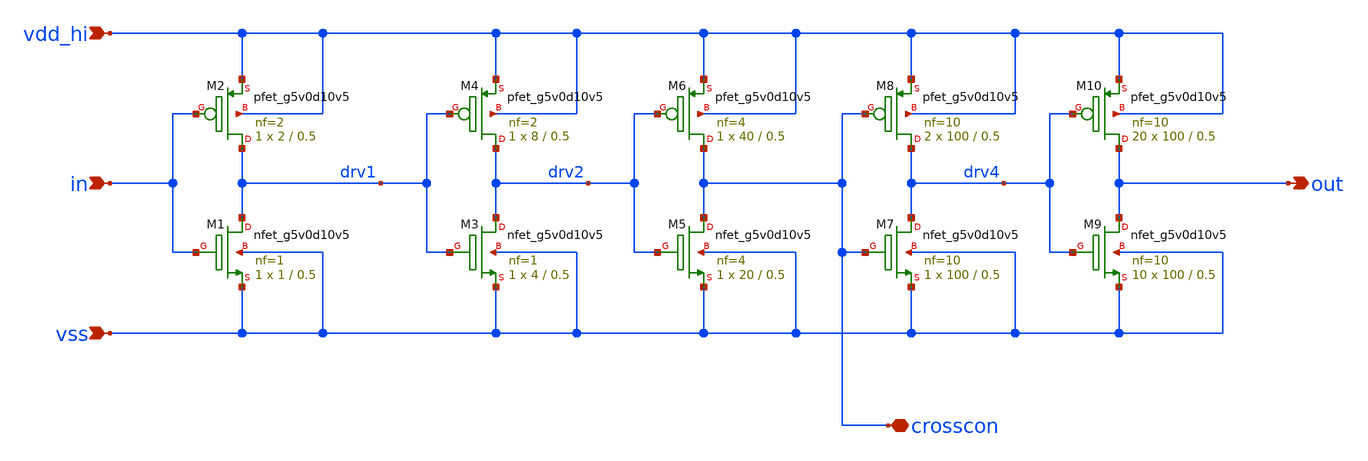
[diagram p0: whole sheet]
** sch_path: xschem/audiodac_drv_half.sch
* (c) 2022 Harald Pretl, IIC, Johannes Kepler University
**.subckt audiodac_drv_half in out vdd_hi vss crosscon
*.ipin in
*.opin out
*.ipin vdd_hi
*.ipin vss
*.iopin crosscon
XM10 out drv4 vdd_hi vdd_hi sky130_fd_pr__pfet_g5v0d10v5 L=0.5 W=100 nf=10 ad='int((10 + 1)/2) * 100 / 10 * 0.29'
+ as='int((10 + 2)/2) * 100 / 10 * 0.29' pd='2*int((10 + 1)/2) * (100 / 10 + 0.29)' ps='2*int((10 + 2)/2) * (100 / 10 + 0.29)'
+ nrd='0.29 / 100 ' nrs='0.29 / 100 ' sa=0 sb=0 sd=0 mult=20 m=20
XM9 out drv4 vss vss sky130_fd_pr__nfet_g5v0d10v5 L=0.5 W=100 nf=10 ad='int((10 + 1)/2) * 100 / 10 * 0.29'
+ as='int((10 + 2)/2) * 100 / 10 * 0.29' pd='2*int((10 + 1)/2) * (100 / 10 + 0.29)' ps='2*int((10 + 2)/2) * (100 / 10 + 0.29)'
+ nrd='0.29 / 100 ' nrs='0.29 / 100 ' sa=0 sb=0 sd=0 mult=10 m=10
XM8 drv4 crosscon vdd_hi vdd_hi sky130_fd_pr__pfet_g5v0d10v5 L=0.5 W=100 nf=10 ad='int((10 + 1)/2) * 100 / 10 * 0.29'
+ as='int((10 + 2)/2) * 100 / 10 * 0.29' pd='2*int((10 + 1)/2) * (100 / 10 + 0.29)' ps='2*int((10 + 2)/2) * (100 / 10 + 0.29)'
+ nrd='0.29 / 100 ' nrs='0.29 / 100 ' sa=0 sb=0 sd=0 mult=2 m=2
XM7 drv4 crosscon vss vss sky130_fd_pr__nfet_g5v0d10v5 L=0.5 W=100 nf=10 ad='int((10 + 1)/2) * 100 / 10 * 0.29'
+ as='int((10 + 2)/2) * 100 / 10 * 0.29' pd='2*int((10 + 1)/2) * (100 / 10 + 0.29)' ps='2*int((10 + 2)/2) * (100 / 10 + 0.29)'
+ nrd='0.29 / 100 ' nrs='0.29 / 100 ' sa=0 sb=0 sd=0 mult=1 m=1
XM6 crosscon drv2 vdd_hi vdd_hi sky130_fd_pr__pfet_g5v0d10v5 L=0.5 W=40 nf=4 ad='int((4 + 1)/2) * 40 / 4 * 0.29'
+ as='int((4 + 2)/2) * 40 / 4 * 0.29' pd='2*int((4 + 1)/2) * (40 / 4 + 0.29)' ps='2*int((4 + 2)/2) * (40 / 4 + 0.29)'
+ nrd='0.29 / 40 ' nrs='0.29 / 40 ' sa=0 sb=0 sd=0 mult=1 m=1
XM5 crosscon drv2 vss vss sky130_fd_pr__nfet_g5v0d10v5 L=0.5 W=20 nf=4 ad='int((4 + 1)/2) * 20 / 4 * 0.29'
+ as='int((4 + 2)/2) * 20 / 4 * 0.29' pd='2*int((4 + 1)/2) * (20 / 4 + 0.29)' ps='2*int((4 + 2)/2) * (20 / 4 + 0.29)'
+ nrd='0.29 / 20 ' nrs='0.29 / 20 ' sa=0 sb=0 sd=0 mult=1 m=1
XM4 drv2 drv1 vdd_hi vdd_hi sky130_fd_pr__pfet_g5v0d10v5 L=0.5 W=8 nf=2 ad='int((2 + 1)/2) * 8 / 2 * 0.29'
+ as='int((2 + 2)/2) * 8 / 2 * 0.29' pd='2*int((2 + 1)/2) * (8 / 2 + 0.29)' ps='2*int((2 + 2)/2) * (8 / 2 + 0.29)'
+ nrd='0.29 / 8 ' nrs='0.29 / 8 ' sa=0 sb=0 sd=0 mult=1 m=1
XM3 drv2 drv1 vss vss sky130_fd_pr__nfet_g5v0d10v5 L=0.5 W=4 nf=1 ad='int((1 + 1)/2) * 4 / 1 * 0.29'
+ as='int((1 + 2)/2) * 4 / 1 * 0.29' pd='2*int((1 + 1)/2) * (4 / 1 + 0.29)' ps='2*int((1 + 2)/2) * (4 / 1 + 0.29)'
+ nrd='0.29 / 4 ' nrs='0.29 / 4 ' sa=0 sb=0 sd=0 mult=1 m=1
XM2 drv1 in vdd_hi vdd_hi sky130_fd_pr__pfet_g5v0d10v5 L=0.5 W=2 nf=2 ad='int((2 + 1)/2) * 2 / 2 * 0.29'
+ as='int((2 + 2)/2) * 2 / 2 * 0.29' pd='2*int((2 + 1)/2) * (2 / 2 + 0.29)' ps='2*int((2 + 2)/2) * (2 / 2 + 0.29)'
+ nrd='0.29 / 2 ' nrs='0.29 / 2 ' sa=0 sb=0 sd=0 mult=1 m=1
XM1 drv1 in vss vss sky130_fd_pr__nfet_g5v0d10v5 L=0.5 W=1 nf=1 ad='int((1 + 1)/2) * 1 / 1 * 0.29' as='int((1 + 2)/2) * 1 / 1 * 0.29'
+ pd='2*int((1 + 1)/2) * (1 / 1 + 0.29)' ps='2*int((1 + 2)/2) * (1 / 1 + 0.29)' nrd='0.29 / 1 ' nrs='0.29 / 1 '
+ sa=0 sb=0 sd=0 mult=1 m=1
**.ends
.end
